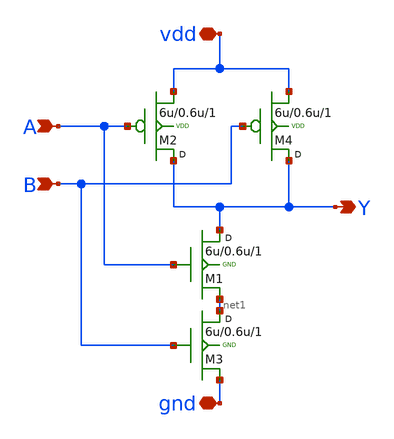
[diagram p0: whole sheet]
** sch_path: Tutorials/1-4_StdCell_DFFSR/Layout/1_NAND2X1_Sch/NAND2X1.sch
**.subckt NAND2X1 A B Y vdd gnd
*.ipin A
*.ipin B
*.opin Y
*.iopin vdd
*.iopin gnd
M1 Y A net1 GND nfet w=6u l=0.6u m=1
M2 Y A vdd VDD pfet w=6u l=0.6u m=1
M3 net1 B gnd GND nfet w=6u l=0.6u m=1
M4 Y B vdd VDD pfet w=6u l=0.6u m=1
**.ends
.end
